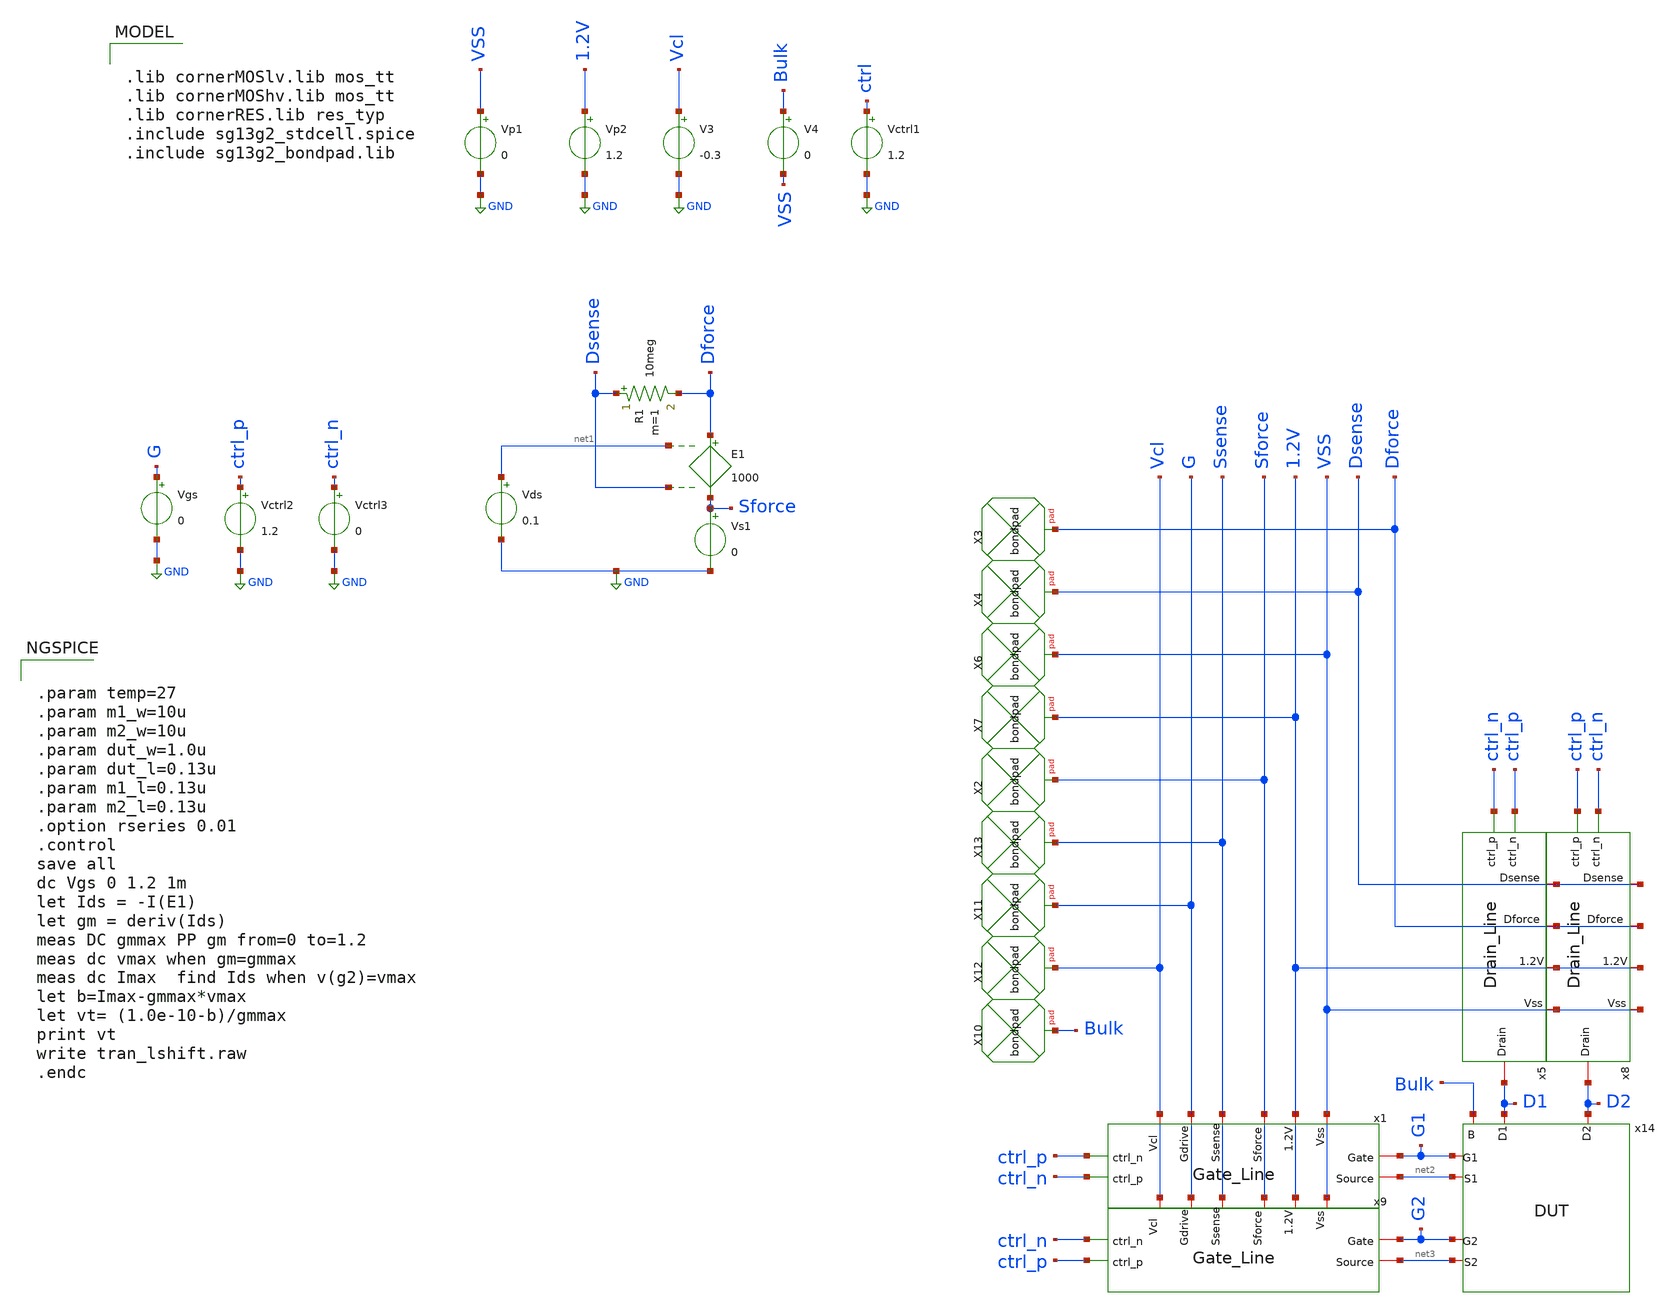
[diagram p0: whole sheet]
** sch_path: design_data/xschem/MissMatch_chip_tb.sch
**.subckt MissMatch_chip_tb
Vp2 1.2V GND 1.2
V3 Vcl GND -0.3
XX2 Sforce bondpad size=80u shape=0 padtype=0
XX3 Dforce bondpad size=80u shape=0 padtype=0
XX4 Dsense bondpad size=80u shape=0 padtype=0
XX6 VSS bondpad size=80u shape=0 padtype=0
XX7 1.2V bondpad size=80u shape=0 padtype=0
Vp1 VSS GND 0
XX10 Bulk bondpad size=80u shape=0 padtype=0
V4 Bulk VSS 0
Vs1 Sforce GND 0
E1 Dforce Sforce net1 Dsense 1000
Vds net1 GND 0.1
R1 Dsense Dforce 10meg m=1
x5 ctrl_p ctrl_n Dsense Dforce 1.2V D1 VSS Drain_Line
x8 ctrl_n ctrl_p Dsense Dforce 1.2V D2 VSS Drain_Line
x1 ctrl_p ctrl_n Vcl G Ssense Sforce 1.2V VSS net2 G1 Gate_Line
x9 ctrl_n ctrl_p Vcl G Ssense Sforce 1.2V VSS net3 G2 Gate_Line
Vctrl1 ctrl GND 1.2
Vgs G GND 0
Vctrl2 ctrl_p GND 1.2
Vctrl3 ctrl_n GND 0
XX13 Ssense bondpad size=80u shape=0 padtype=0
XX11 G bondpad size=80u shape=0 padtype=0
XX12 Vcl bondpad size=80u shape=0 padtype=0
x14 Bulk D2 D1 G1 net2 G2 net3 DUT
**** begin user architecture code

.lib cornerMOSlv.lib mos_tt
.lib cornerMOShv.lib mos_tt
.lib cornerRES.lib res_typ
.include sg13g2_stdcell.spice
.include sg13g2_bondpad.lib



.param temp=27
.param m1_w=10u
.param m2_w=10u
.param dut_w=1.0u
.param dut_l=0.13u
.param m1_l=0.13u
.param m2_l=0.13u
.option rseries 0.01
.control
save all
dc Vgs 0 1.2 1m
let Ids = -I(E1)
let gm = deriv(Ids)
meas DC gmmax PP gm from=0 to=1.2
meas dc vmax when gm=gmmax
meas dc Imax  find Ids when v(g2)=vmax
let b=Imax-gmmax*vmax
let vt= (1.0e-10-b)/gmmax
print vt
write tran_lshift.raw
.endc


**** end user architecture code
**.ends

* expanding   symbol:  Drain_Line.sym # of pins=7
** sym_path: Drain_Line.sym
** sch_path: Drain_Line.sch
.subckt Drain_Line ctrl_n ctrl_p Dsense Dforce 1.2V Drain Vss
*.iopin Vss
*.ipin ctrl_n
*.iopin 1.2V
*.iopin Dsense
*.iopin Drain
*.iopin Dforce
*.ipin ctrl_p
XM4 Dsense ctrl_p Drain net4 sg13_lv_nmos w=0.15u l=0.13u ng=1 m=1 mm_ok=1
XM8 Drain ctrl_n Dsense net3 sg13_lv_pmos w=0.30u l=0.13u ng=1 m=1 mm_ok=1
XM9 Drain ctrl_n Dforce net2 sg13_lv_pmos w={m2_w} l=0.13u ng=1 m=1 mm_ok=1
XM10 Dforce ctrl_p Drain net1 sg13_lv_nmos w={m1_w} l=0.13u ng=1 m=1 mm_ok=1
XR1 Vss net4 ptap1 R=30.62 w=10.0e-6 l=1.0e-6
XR2 1.2V net2 ntap1 R=12.73 w=25.0e-6 l=1.0e-6
XR3 Vss net1 ptap1 R=12.73 w=25.0e-6 l=1.0e-6
XR4 1.2V net3 ntap1 R=30.62 w=10.0e-6 l=1.0e-6
.ends


* expanding   symbol:  Gate_Line.sym # of pins=10
** sym_path: Gate_Line.sym
** sch_path: Gate_Line.sch
.subckt Gate_Line ctrl_n ctrl_p Vcl Gdrive Ssense Sforce 1.2V Vss Source Gate
*.iopin Gate
*.iopin Vss
*.iopin Gdrive
*.ipin ctrl_p
*.iopin 1.2V
*.iopin Vcl
*.iopin Ssense
*.iopin Source
*.iopin Sforce
*.ipin ctrl_n
XM1 Gate ctrl_n Gdrive net5 sg13_lv_pmos w=0.30u l=0.13u ng=1 m=1 mm_ok=1
XM2 Gdrive ctrl_p Gate net1 sg13_lv_nmos w=0.15u l=0.13u ng=1 m=1 mm_ok=1
XM3 Vcl ctrl_n Gate net2 sg13_lv_nmos w=0.35u l=0.13u ng=1 m=1 mm_ok=1
XM4 Source ctrl_n Ssense net3 sg13_lv_pmos w=0.30u l=0.13u ng=1 m=1 mm_ok=1
XM5 Ssense ctrl_p Source net4 sg13_lv_nmos w=0.15u l=0.13u ng=1 m=1 mm_ok=1
XM6 Source ctrl_n Sforce net7 sg13_lv_pmos w={m2_w} l=0.13u ng=1 m=1 mm_ok=1
XM7 Sforce ctrl_p Source net6 sg13_lv_nmos w={m1_w} l=0.13u ng=1 m=1 mm_ok=1
XR1 Vss net1 ptap1 R=33.38 w=10.0e-6 l=0.78e-6
XR2 1.2V net5 ntap1 R=33.38 w=10.0e-6 l=0.78e-6
XR3 Vss net2 ptap1 R=33.38 w=10.0e-6 l=0.78e-6
XR4 Vss net4 ptap1 R=33.38 w=10.0e-6 l=0.78e-6
XR5 1.2V net3 ntap1 R=33.38 w=10.0e-6 l=0.78e-6
XR6 Vss net6 ptap1 R=33.38 w=10.0e-6 l=0.78e-6
XR7 1.2V net7 ntap1 R=33.38 w=10.0e-6 l=0.78e-6
.ends


* expanding   symbol:  DUT.sym # of pins=7
** sym_path: design_data/xschem/DUT.sym
** sch_path: design_data/xschem/DUT.sch
.subckt DUT B D2 D1 G1 S1 G2 S2
*.iopin S1
*.iopin G1
*.iopin D1
*.iopin B
*.iopin S2
*.iopin G2
*.iopin D2
XM1 D1 G1 S1 net1 sg13_lv_nmos w={dut_w} l={dut_l} ng=1 m=1 mm_ok=1
XR3 B net1 ptap1 R=33.38 w=10.0e-6 l=0.78e-6
XM2 D2 G1 S1 net2 sg13_lv_nmos w={dut_w} l={dut_l} ng=1 m=1 mm_ok=1
XR1 B net2 ptap1 R=33.38 w=10.0e-6 l=0.78e-6
XM3 D1 G2 S2 net3 sg13_lv_nmos w={dut_w} l={dut_l} ng=1 m=1 mm_ok=1
XR2 B net3 ptap1 R=33.38 w=10.0e-6 l=0.78e-6
XM4 D2 G2 S2 net4 sg13_lv_nmos w={dut_w} l={dut_l} ng=1 m=1 mm_ok=1
XR4 B net4 ptap1 R=33.38 w=10.0e-6 l=0.78e-6
.ends

.GLOBAL GND
.end
